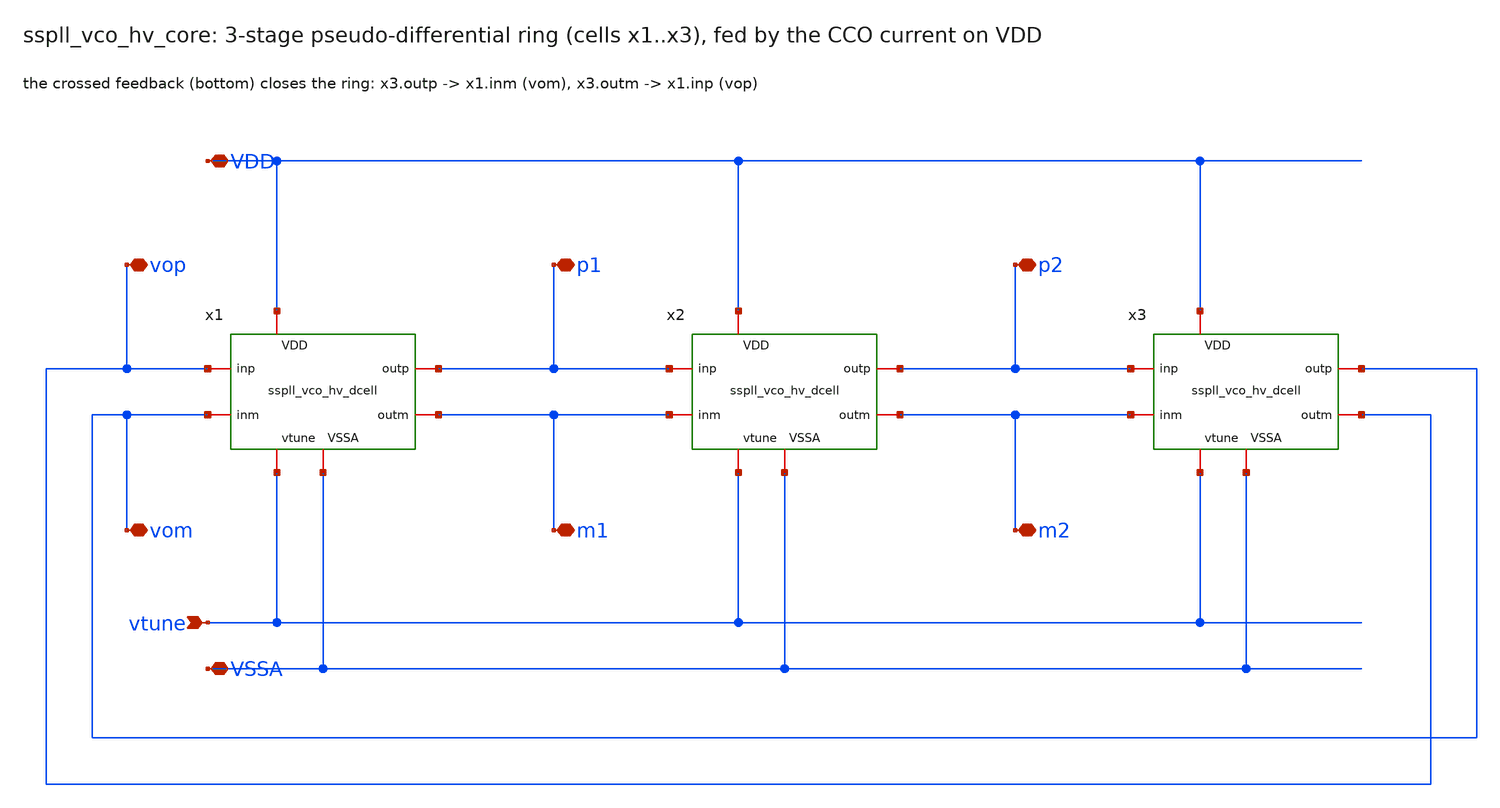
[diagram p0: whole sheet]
** sch_path: xschem/vco_hv/sspll_vco_hv_core.sch
**.subckt sspll_vco_hv_core VDD vtune VSSA p1 m1 p2 m2 vop vom
*.iopin VDD
*.ipin vtune
*.iopin VSSA
*.iopin p1
*.iopin m1
*.iopin p2
*.iopin m2
*.iopin vop
*.iopin vom
x1 vop vom p1 m1 VDD vtune VSSA sspll_vco_hv_dcell
x2 p1 m1 p2 m2 VDD vtune VSSA sspll_vco_hv_dcell
x3 p2 m2 vom vop VDD vtune VSSA sspll_vco_hv_dcell
**.ends

* expanding   symbol:  sspll_vco_hv_dcell.sym # of pins=7
** sym_path: xschem/vco_hv/sspll_vco_hv_dcell.sym
** sch_path: xschem/vco_hv/sspll_vco_hv_dcell.sch
.subckt sspll_vco_hv_dcell inp inm outp outm VDD vtune VSSA
*.iopin VDD
*.iopin VSSA
*.ipin vtune
*.ipin inp
*.ipin inm
*.opin outm
*.opin outp
XXP1 outm inp VDD VDD sky130_fd_pr__pfet_g5v0d10v5 L=0.5 W=25 nf=5 ad='int((nf+1)/2) * W/nf * 0.29' as='int((nf+2)/2) * W/nf * 0.29'
+ pd='2*int((nf+1)/2) * (W/nf + 0.29)' ps='2*int((nf+2)/2) * (W/nf + 0.29)' nrd='0.29 / W' nrs='0.29 / W'
+ sa=0 sb=0 sd=0 mult=1 m=1
XXN1 outm inp VSSA VSSA sky130_fd_pr__nfet_g5v0d10v5 L=0.5 W=7.5 nf=2 ad='int((nf+1)/2) * W/nf * 0.29'
+ as='int((nf+2)/2) * W/nf * 0.29' pd='2*int((nf+1)/2) * (W/nf + 0.29)' ps='2*int((nf+2)/2) * (W/nf + 0.29)'
+ nrd='0.29 / W' nrs='0.29 / W' sa=0 sb=0 sd=0 mult=1 m=1
XXS1 outm vtune net1 VSSA sky130_fd_pr__nfet_g5v0d10v5 L=1.0 W=10 nf=2 ad='int((nf+1)/2) * W/nf * 0.29'
+ as='int((nf+2)/2) * W/nf * 0.29' pd='2*int((nf+1)/2) * (W/nf + 0.29)' ps='2*int((nf+2)/2) * (W/nf + 0.29)'
+ nrd='0.29 / W' nrs='0.29 / W' sa=0 sb=0 sd=0 mult=1 m=1
XXC1 VSSA net1 VSSA VSSA sky130_fd_pr__nfet_g5v0d10v5 L=1.0 W=6.25 nf=1 ad='int((nf+1)/2) * W/nf * 0.29'
+ as='int((nf+2)/2) * W/nf * 0.29' pd='2*int((nf+1)/2) * (W/nf + 0.29)' ps='2*int((nf+2)/2) * (W/nf + 0.29)'
+ nrd='0.29 / W' nrs='0.29 / W' sa=0 sb=0 sd=0 mult=1 m=1
XXP2 outp inm VDD VDD sky130_fd_pr__pfet_g5v0d10v5 L=0.5 W=25 nf=5 ad='int((nf+1)/2) * W/nf * 0.29' as='int((nf+2)/2) * W/nf * 0.29'
+ pd='2*int((nf+1)/2) * (W/nf + 0.29)' ps='2*int((nf+2)/2) * (W/nf + 0.29)' nrd='0.29 / W' nrs='0.29 / W'
+ sa=0 sb=0 sd=0 mult=1 m=1
XXN2 outp inm VSSA VSSA sky130_fd_pr__nfet_g5v0d10v5 L=0.5 W=7.5 nf=2 ad='int((nf+1)/2) * W/nf * 0.29'
+ as='int((nf+2)/2) * W/nf * 0.29' pd='2*int((nf+1)/2) * (W/nf + 0.29)' ps='2*int((nf+2)/2) * (W/nf + 0.29)'
+ nrd='0.29 / W' nrs='0.29 / W' sa=0 sb=0 sd=0 mult=1 m=1
XXS2 outp vtune net2 VSSA sky130_fd_pr__nfet_g5v0d10v5 L=1.0 W=10 nf=2 ad='int((nf+1)/2) * W/nf * 0.29'
+ as='int((nf+2)/2) * W/nf * 0.29' pd='2*int((nf+1)/2) * (W/nf + 0.29)' ps='2*int((nf+2)/2) * (W/nf + 0.29)'
+ nrd='0.29 / W' nrs='0.29 / W' sa=0 sb=0 sd=0 mult=1 m=1
XXC2 VSSA net2 VSSA VSSA sky130_fd_pr__nfet_g5v0d10v5 L=1.0 W=6.25 nf=1 ad='int((nf+1)/2) * W/nf * 0.29'
+ as='int((nf+2)/2) * W/nf * 0.29' pd='2*int((nf+1)/2) * (W/nf + 0.29)' ps='2*int((nf+2)/2) * (W/nf + 0.29)'
+ nrd='0.29 / W' nrs='0.29 / W' sa=0 sb=0 sd=0 mult=1 m=1
XXT1N inp VDD outp VSSA sky130_fd_pr__nfet_g5v0d10v5 L=1.0 W=3.75 nf=2 ad='int((nf+1)/2) * W/nf * 0.29'
+ as='int((nf+2)/2) * W/nf * 0.29' pd='2*int((nf+1)/2) * (W/nf + 0.29)' ps='2*int((nf+2)/2) * (W/nf + 0.29)'
+ nrd='0.29 / W' nrs='0.29 / W' sa=0 sb=0 sd=0 mult=1 m=1
XXT1P outp VSSA inp VDD sky130_fd_pr__pfet_g5v0d10v5 L=0.5 W=7.5 nf=2 ad='int((nf+1)/2) * W/nf * 0.29'
+ as='int((nf+2)/2) * W/nf * 0.29' pd='2*int((nf+1)/2) * (W/nf + 0.29)' ps='2*int((nf+2)/2) * (W/nf + 0.29)'
+ nrd='0.29 / W' nrs='0.29 / W' sa=0 sb=0 sd=0 mult=1 m=1
XXT2N inm VDD outm VSSA sky130_fd_pr__nfet_g5v0d10v5 L=1.0 W=3.75 nf=2 ad='int((nf+1)/2) * W/nf * 0.29'
+ as='int((nf+2)/2) * W/nf * 0.29' pd='2*int((nf+1)/2) * (W/nf + 0.29)' ps='2*int((nf+2)/2) * (W/nf + 0.29)'
+ nrd='0.29 / W' nrs='0.29 / W' sa=0 sb=0 sd=0 mult=1 m=1
XXT2P outm VSSA inm VDD sky130_fd_pr__pfet_g5v0d10v5 L=0.5 W=7.5 nf=2 ad='int((nf+1)/2) * W/nf * 0.29'
+ as='int((nf+2)/2) * W/nf * 0.29' pd='2*int((nf+1)/2) * (W/nf + 0.29)' ps='2*int((nf+2)/2) * (W/nf + 0.29)'
+ nrd='0.29 / W' nrs='0.29 / W' sa=0 sb=0 sd=0 mult=1 m=1
.ends

.end
